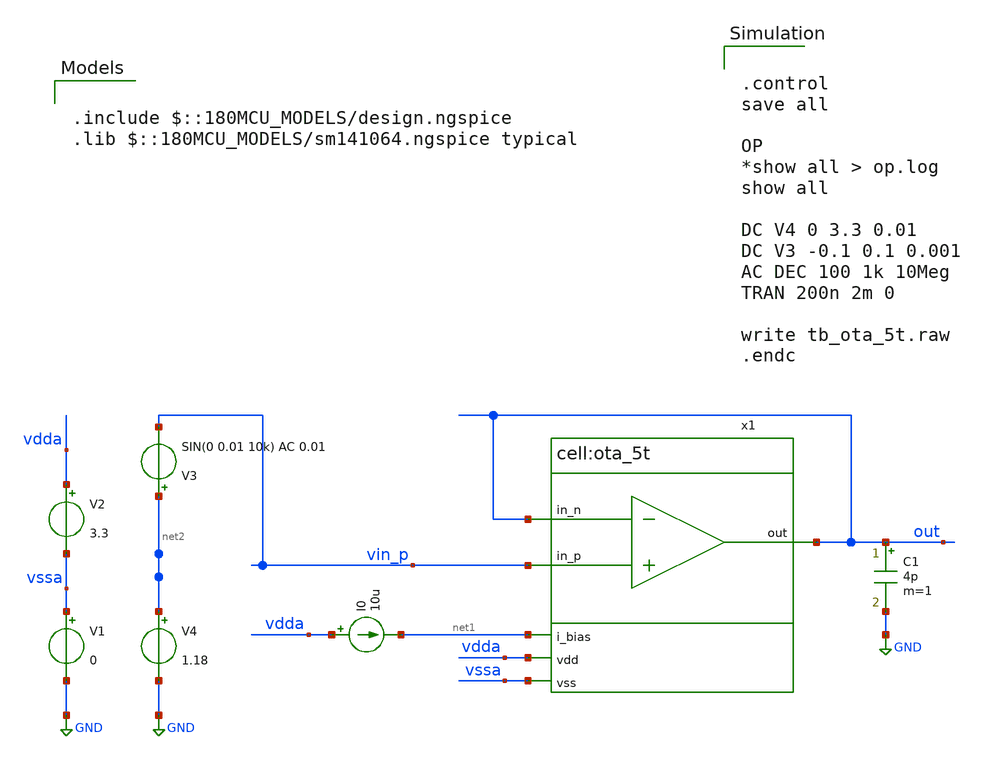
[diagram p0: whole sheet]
** sch_path: designs/libs/tb_analog/tb_ota_5t_dc/tb_ota_5t_dc.sch
**.subckt tb_ota_5t_dc
V1 vssa GND 0
V2 vdda vssa 3.3
I0 vdda net1 10u
V3 net2 vin_p SIN(0 0.01 10k) AC 0.01
x1 vdda out vin_p out net1 vssa ota_5t
V4 net2 GND 1.18
C1 out GND 4p m=1
**** begin user architecture code


.control
save all

OP
*show all > op.log
show all

DC V4 0 3.3 0.01
DC V3 -0.1 0.1 0.001
AC DEC 100 1k 10Meg
TRAN 200n 2m 0

write tb_ota_5t.raw
.endc



.include $::180MCU_MODELS/design.ngspice
.lib $::180MCU_MODELS/sm141064.ngspice typical

**** end user architecture code
**.ends

* expanding   symbol:  libs/core_analog/ota_5t/ota_5t.sym # of pins=6
** sym_path: libs/core_analog/ota_5t/ota_5t.sym
** sch_path: libs/core_analog/ota_5t/ota_5t.sch
.subckt ota_5t vdd out in_p in_n i_bias vss
*.ipin in_p
*.ipin in_n
*.ipin i_bias
*.ipin vdd
*.ipin vss
*.opin out
XM1 net2 i_bias vss vss nfet_03v3 L=1u W=2.5u nf=1 ad='int((nf+1)/2) * W/nf * 0.18u' as='int((nf+2)/2) * W/nf * 0.18u'
+ pd='2*int((nf+1)/2) * (W/nf + 0.18u)' ps='2*int((nf+2)/2) * (W/nf + 0.18u)' nrd='0.18u / W' nrs='0.18u / W'
+ sa=0 sb=0 sd=0 m=1
XM2 i_bias i_bias vss vss nfet_03v3 L=1u W=2.5u nf=1 ad='int((nf+1)/2) * W/nf * 0.18u' as='int((nf+2)/2) * W/nf * 0.18u'
+ pd='2*int((nf+1)/2) * (W/nf + 0.18u)' ps='2*int((nf+2)/2) * (W/nf + 0.18u)' nrd='0.18u / W' nrs='0.18u / W'
+ sa=0 sb=0 sd=0 m=1
XM3 net1 in_p net2 vss nfet_03v3 L=1u W=4.5u nf=2 ad='int((nf+1)/2) * W/nf * 0.18u' as='int((nf+2)/2) * W/nf * 0.18u'
+ pd='2*int((nf+1)/2) * (W/nf + 0.18u)' ps='2*int((nf+2)/2) * (W/nf + 0.18u)' nrd='0.18u / W' nrs='0.18u / W'
+ sa=0 sb=0 sd=0 m=1
XM4 out in_n net2 vss nfet_03v3 L=1u W=4.5u nf=2 ad='int((nf+1)/2) * W/nf * 0.18u' as='int((nf+2)/2) * W/nf * 0.18u'
+ pd='2*int((nf+1)/2) * (W/nf + 0.18u)' ps='2*int((nf+2)/2) * (W/nf + 0.18u)' nrd='0.18u / W' nrs='0.18u / W'
+ sa=0 sb=0 sd=0 m=1
XM5 out net1 vdd vdd pfet_03v3 L=1u W=5.5u nf=1 ad='int((nf+1)/2) * W/nf * 0.18u' as='int((nf+2)/2) * W/nf * 0.18u'
+ pd='2*int((nf+1)/2) * (W/nf + 0.18u)' ps='2*int((nf+2)/2) * (W/nf + 0.18u)' nrd='0.18u / W' nrs='0.18u / W'
+ sa=0 sb=0 sd=0 m=1
XM6 net1 net1 vdd vdd pfet_03v3 L=1u W=5.5u nf=1 ad='int((nf+1)/2) * W/nf * 0.18u' as='int((nf+2)/2) * W/nf * 0.18u'
+ pd='2*int((nf+1)/2) * (W/nf + 0.18u)' ps='2*int((nf+2)/2) * (W/nf + 0.18u)' nrd='0.18u / W' nrs='0.18u / W'
+ sa=0 sb=0 sd=0 m=1
.ends

.GLOBAL GND
.end
